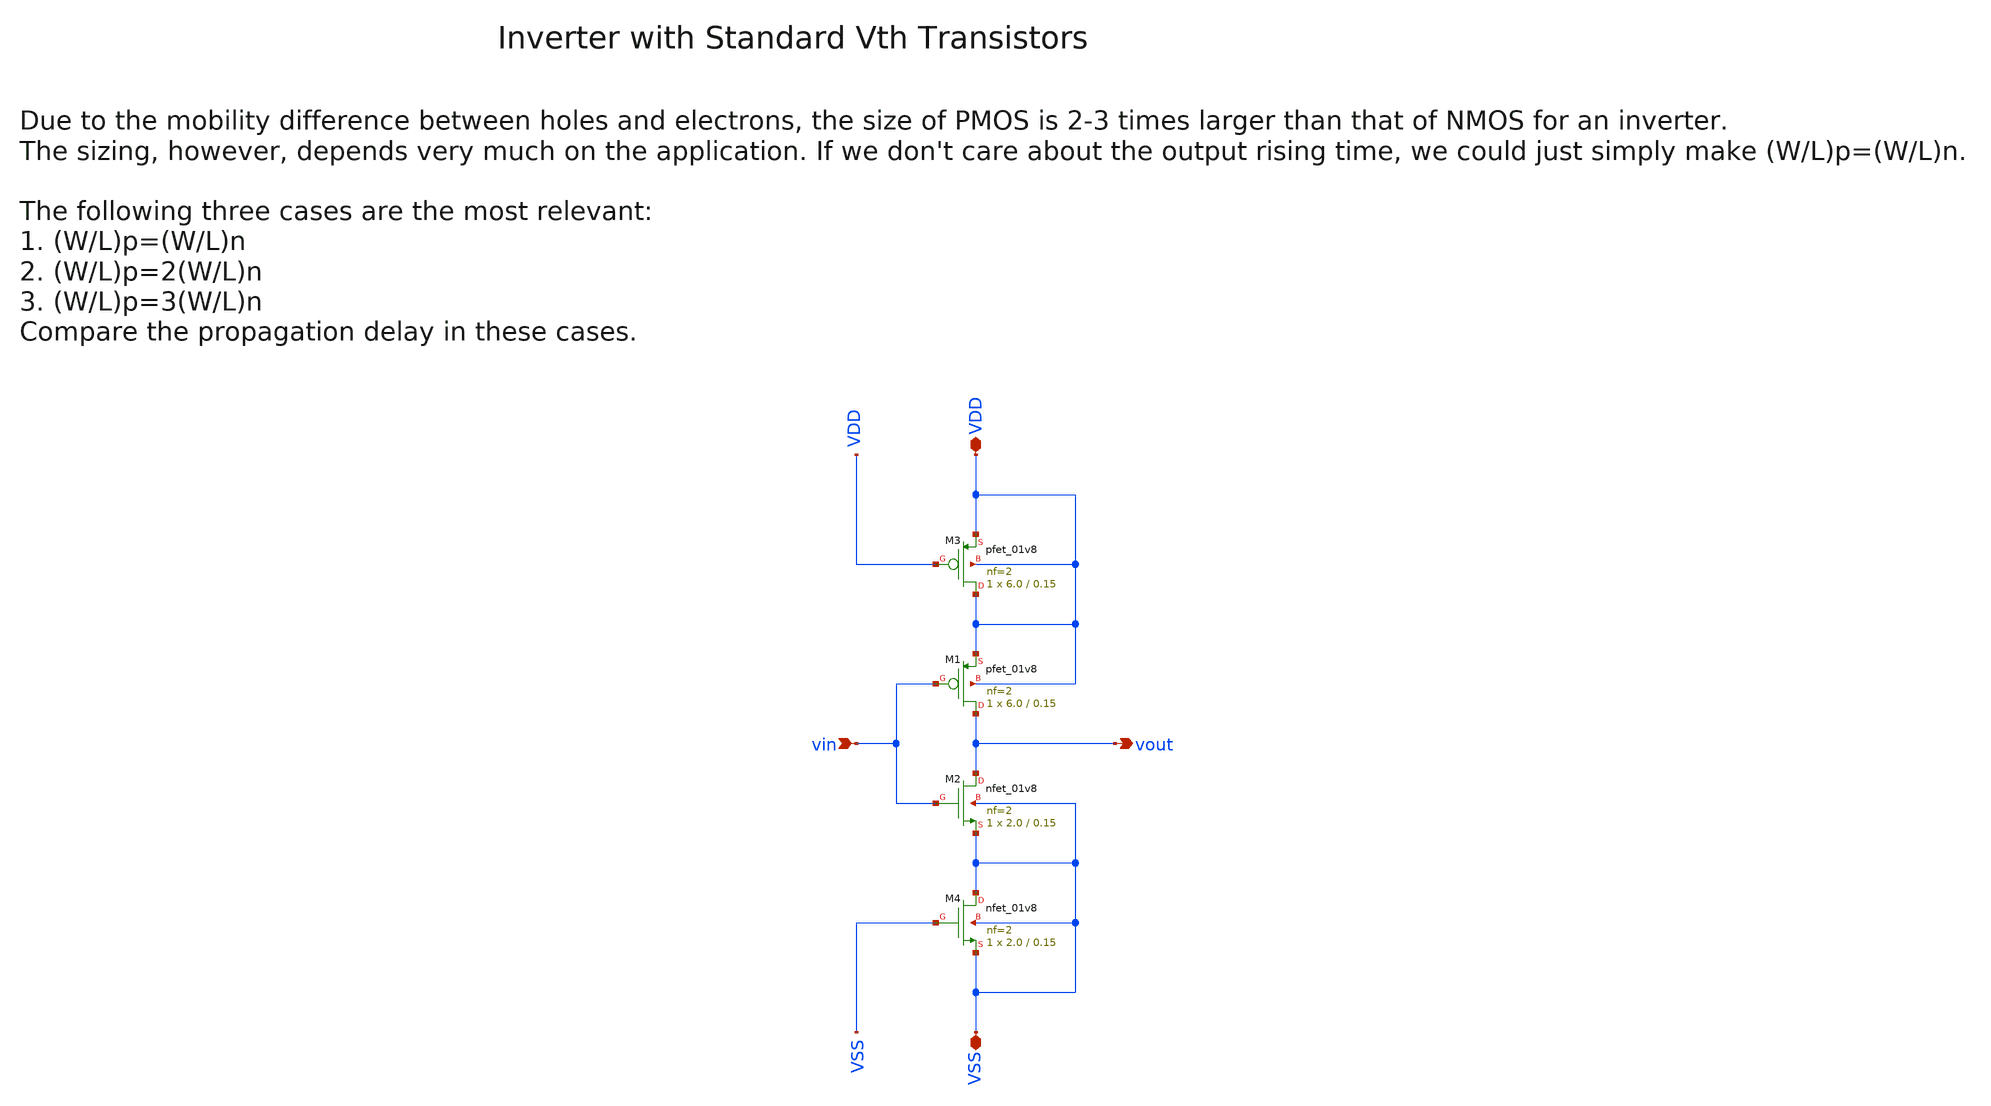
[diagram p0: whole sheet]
** sch_path: sky130/macros/iqmod/schematic/wspr_tx_iqmod_mixer_lo_logic_inv_NF2.sch
**.subckt wspr_tx_iqmod_mixer_lo_logic_inv_NF2 vin VDD VSS vout
*.ipin vin
*.iopin VDD
*.iopin VSS
*.opin vout
XM1 vout vin VDD VDD sky130_fd_pr__pfet_01v8 L=0.15 W=6.0 nf=2 ad='int((2 + 1)/2) * 6.0 / 2 * 0.29' as='int((2 + 2)/2) * 6.0 / 2 * 0.29'
+ pd='2*int((2 + 1)/2) * (6.0 / 2 + 0.29)' ps='2*int((2 + 2)/2) * (6.0 / 2 + 0.29)' nrd='0.29 / 6.0 ' nrs='0.29 / 6.0 '
+ sa=0 sb=0 sd=0 mult=1 m=1
XM3 VDD VDD VDD VDD sky130_fd_pr__pfet_01v8 L=0.15 W=6.0 nf=2 ad='int((2 + 1)/2) * 6.0 / 2 * 0.29' as='int((2 + 2)/2) * 6.0 / 2 * 0.29'
+ pd='2*int((2 + 1)/2) * (6.0 / 2 + 0.29)' ps='2*int((2 + 2)/2) * (6.0 / 2 + 0.29)' nrd='0.29 / 6.0 ' nrs='0.29 / 6.0 '
+ sa=0 sb=0 sd=0 mult=1 m=1
XM2 vout vin VSS VSS sky130_fd_pr__nfet_01v8 L=0.15 W=2.0 nf=2 ad='int((2 + 1)/2) * 2.0 / 2 * 0.29' as='int((2 + 2)/2) * 2.0 / 2 * 0.29'
+ pd='2*int((2 + 1)/2) * (2.0 / 2 + 0.29)' ps='2*int((2 + 2)/2) * (2.0 / 2 + 0.29)' nrd='0.29 / 2.0 ' nrs='0.29 / 2.0 '
+ sa=0 sb=0 sd=0 mult=1 m=1
XM4 VSS VSS VSS VSS sky130_fd_pr__nfet_01v8 L=0.15 W=2.0 nf=2 ad='int((2 + 1)/2) * 2.0 / 2 * 0.29' as='int((2 + 2)/2) * 2.0 / 2 * 0.29'
+ pd='2*int((2 + 1)/2) * (2.0 / 2 + 0.29)' ps='2*int((2 + 2)/2) * (2.0 / 2 + 0.29)' nrd='0.29 / 2.0 ' nrs='0.29 / 2.0 '
+ sa=0 sb=0 sd=0 mult=1 m=1
**.ends
.end
